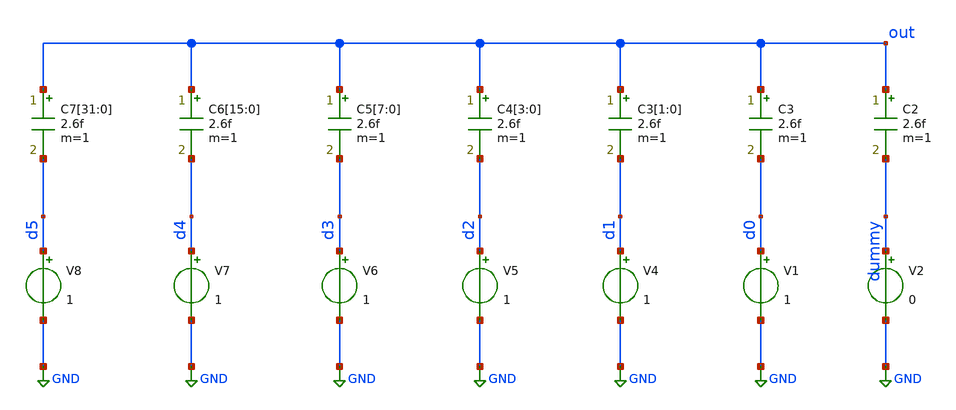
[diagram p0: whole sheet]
** sch_path: xschem/tb/cdac/tb_cdac.sch
**.subckt tb_cdac
V4 d1 GND 1
V5 d2 GND 1
V6 d3 GND 1
V7 d4 GND 1
V8 d5 GND 1
C2 out dummy 2.6f m=1
C3 out d0 2.6f m=1
C3[1] out d1 2.6f m=1
C3[0] out d1 2.6f m=1
C4[3] out d2 2.6f m=1
C4[2] out d2 2.6f m=1
C4[1] out d2 2.6f m=1
C4[0] out d2 2.6f m=1
C5[7] out d3 2.6f m=1
C5[6] out d3 2.6f m=1
C5[5] out d3 2.6f m=1
C5[4] out d3 2.6f m=1
C5[3] out d3 2.6f m=1
C5[2] out d3 2.6f m=1
C5[1] out d3 2.6f m=1
C5[0] out d3 2.6f m=1
C6[15] out d4 2.6f m=1
C6[14] out d4 2.6f m=1
C6[13] out d4 2.6f m=1
C6[12] out d4 2.6f m=1
C6[11] out d4 2.6f m=1
C6[10] out d4 2.6f m=1
C6[9] out d4 2.6f m=1
C6[8] out d4 2.6f m=1
C6[7] out d4 2.6f m=1
C6[6] out d4 2.6f m=1
C6[5] out d4 2.6f m=1
C6[4] out d4 2.6f m=1
C6[3] out d4 2.6f m=1
C6[2] out d4 2.6f m=1
C6[1] out d4 2.6f m=1
C6[0] out d4 2.6f m=1
C7[31] out d5 2.6f m=1
C7[30] out d5 2.6f m=1
C7[29] out d5 2.6f m=1
C7[28] out d5 2.6f m=1
C7[27] out d5 2.6f m=1
C7[26] out d5 2.6f m=1
C7[25] out d5 2.6f m=1
C7[24] out d5 2.6f m=1
C7[23] out d5 2.6f m=1
C7[22] out d5 2.6f m=1
C7[21] out d5 2.6f m=1
C7[20] out d5 2.6f m=1
C7[19] out d5 2.6f m=1
C7[18] out d5 2.6f m=1
C7[17] out d5 2.6f m=1
C7[16] out d5 2.6f m=1
C7[15] out d5 2.6f m=1
C7[14] out d5 2.6f m=1
C7[13] out d5 2.6f m=1
C7[12] out d5 2.6f m=1
C7[11] out d5 2.6f m=1
C7[10] out d5 2.6f m=1
C7[9] out d5 2.6f m=1
C7[8] out d5 2.6f m=1
C7[7] out d5 2.6f m=1
C7[6] out d5 2.6f m=1
C7[5] out d5 2.6f m=1
C7[4] out d5 2.6f m=1
C7[3] out d5 2.6f m=1
C7[2] out d5 2.6f m=1
C7[1] out d5 2.6f m=1
C7[0] out d5 2.6f m=1
V1 d0 GND 1
V2 dummy GND 0
**** begin user architecture code
 *.options method trap
*.options gmin 1e-15
*.options abstol 1e-15
*.options reltol 0.0001
*.options vntol 0.1e-6
*
*.include $::DESIGN_PATH/switches/bootstrapped_sw.sp


.param MC_SWITCH=0

*.tran 100e-9 4e-6
.temp 85


*.tran 100e-9 13e-6 uic
*.tran 10u 10m

.dc V1 0 1 0.1


*loop
.ic V(d5) = 0
.ic V(d4) = 0
.ic V(d3) = 0
.ic V(d2) = 0
.ic V(d1) = 0
.ic V(d0) = 0
.ic V(dummy) = 0
.ic V(out) = 0


.op
run
.control
save all


.endc

 * FET CORNERS
.include $::SKYWATER_MODELS/models/corners/tt.spice
*.include $::SKYWATER_MODELS//corners/ff.spice
*.include $::SKYWATER_MODELS/corners/ss.spice
*.include $::SKYWATER_MODELS/corners/sf.spice
*.include $::SKYWATER_MODELS/corners/fs.spice

* TT + R + C
*.include $::SKYWATER_MODELS/corners/tt_rmax_cmax.spice
*.include $::SKYWATER_MODELS/corners/tt_rmin_cmin.spice
*.include $::SKYWATER_MODELS/corners/tt_rmax_cmin.spice
*.include $::SKYWATER_MODELS/corners/tt_rmin_cmax.spice

* FF + R + C
*.include $::SKYWATER_MODELS/corners/ff_rmax_cmax.spice
*.include $::SKYWATER_MODELS/corners/ff_rmin_cmin.spice
*.include $::SKYWATER_MODELS/corners/ff_rmax_cmin.spice
*.include $::SKYWATER_MODELS/corners/ff_rmin_cmax.spice


* SS + R + C
*.include $::SKYWATER_MODELS/corners/ss_rmax_cmax.spice
*.include $::SKYWATER_MODELS/corners/ss_rmin_cmin.spice
*.include $::SKYWATER_MODELS/corners/ss_rmax_cmin.spice
*.include $::SKYWATER_MODELS/corners/ss_rmin_cmax.spice

* SF + R + C
*.include $::SKYWATER_MODELS/corners/sf_rmax_cmax.spice
*.include $::SKYWATER_MODELS/corners/sf_rmin_cmin.spice
*.include $::SKYWATER_MODELS/corners/sf_rmax_cmin.spice
*.include $::SKYWATER_MODELS/corners/sf_rmin_cmax.spice

* FS + R + C
*.include $::SKYWATER_MODELS/corners/fs_rmax_cmax.spice
*.include $::SKYWATER_MODELS/corners/fs_rmin_cmin.spice
*.include $::SKYWATER_MODELS/corners/fs_rmax_cmin.spice
*.include $::SKYWATER_MODELS/corners/fs_rmin_cmax.spice

**** end user architecture code
**.ends
.GLOBAL GND
.end
